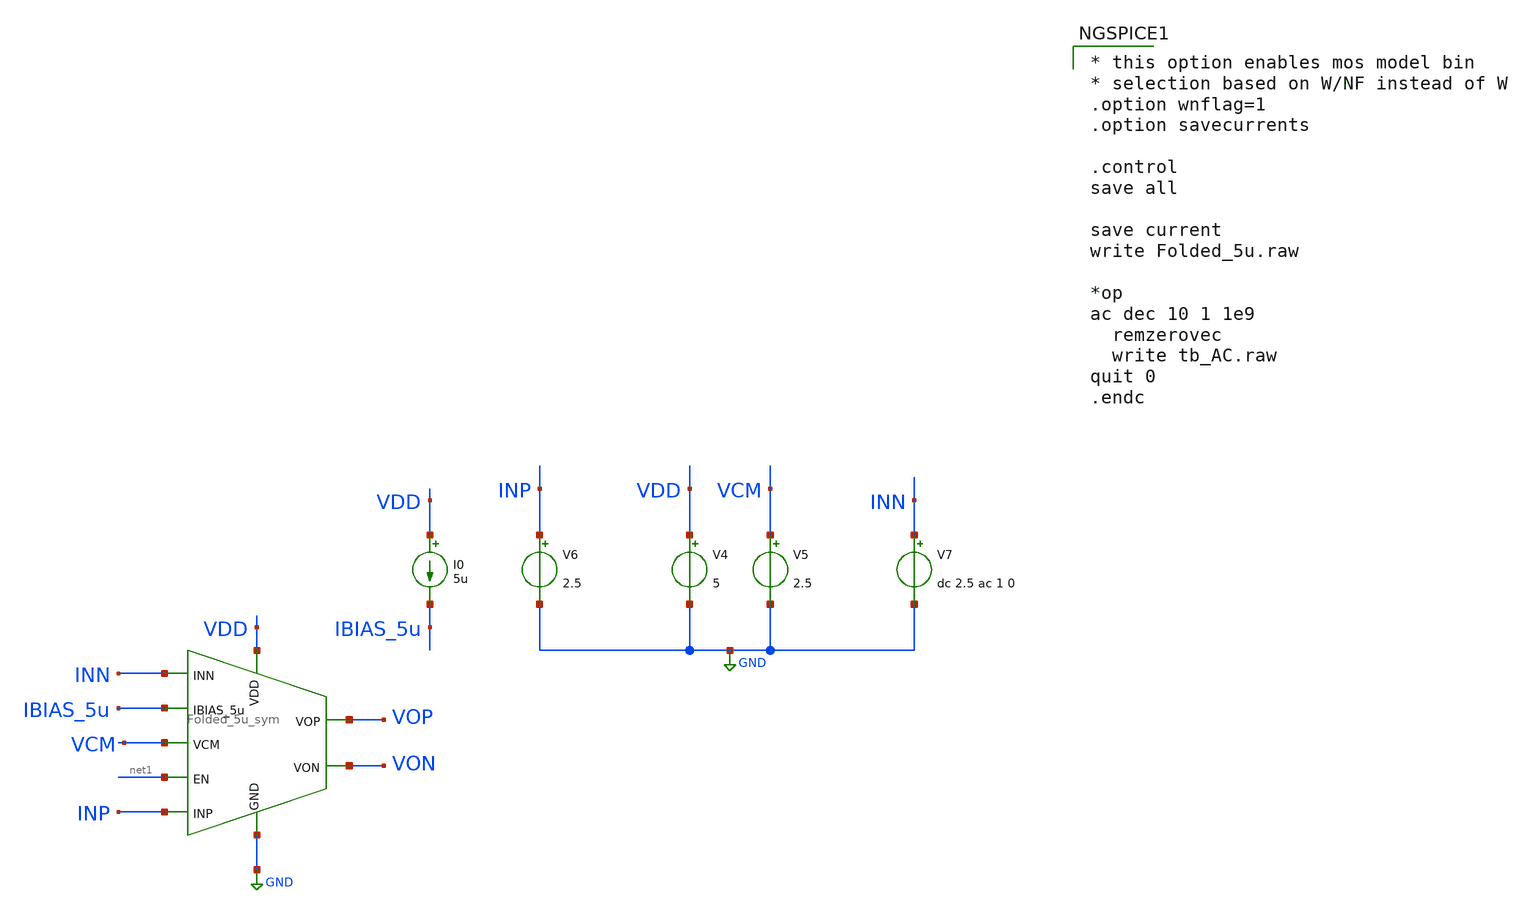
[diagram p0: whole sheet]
** sch_path: Xschem_UPDATE/tb_AC.sch
**.subckt tb_AC
x1 VDD VCM INN INP VOP VON IBIAS_5u net1 GND Folded_5u_sym
I0 VDD IBIAS_5u 5u
V4 VDD GND 5
V6 INP GND 2.5
V5 VCM GND 2.5
V7 INN GND dc 2.5 ac 1 0
**** begin user architecture code

* this option enables mos model bin
* selection based on W/NF instead of W
.option wnflag=1
.option savecurrents

.control
save all

save current
write Folded_5u.raw

*op
ac dec 10 1 1e9
  remzerovec
  write tb_AC.raw
quit 0
.endc


**** end user architecture code
**.ends

* expanding   symbol:  /home/truong/Truong_schem/Folded_5u_sym.sym # of pins=9
** sym_path: Xschem/Folded_5u_sym.sym
** sch_path: Xschem/Folded_5u_sym.sch
.subckt Folded_5u_sym VDD VCM INN INP VOP VON IBIAS_5u EN GND
*.opin VOP
*.opin VON
*.ipin VDD
*.ipin GND
*.ipin IBIAS_5u
*.ipin EN
*.ipin INN
*.ipin INP
*.ipin VCM
*.ipin GND
*.ipin GND
*.ipin GND
*.ipin GND
*.ipin GND
*.ipin IBIAS_5u
*.ipin IBIAS_5u
*.ipin IBIAS_5u
*.ipin VDD
*.ipin VDD
*.ipin VDD
*.ipin VDD
*.ipin VDD
XM13 D13 D13 GND GND sky130_fd_pr__nfet_g5v0d10v5 L=5 W=8 nf=1 ad='int((nf+1)/2) * W/nf * 0.29' as='int((nf+2)/2) * W/nf * 0.29'
+ pd='2*int((nf+1)/2) * (W/nf + 0.29)' ps='2*int((nf+2)/2) * (W/nf + 0.29)' nrd='0.29 / W' nrs='0.29 / W'
+ sa=0 sb=0 sd=0 mult=2 m=2
XM12 VB2 IBIAS_5u GND GND sky130_fd_pr__nfet_g5v0d10v5 L=12 W=2 nf=1 ad='int((nf+1)/2) * W/nf * 0.29'
+ as='int((nf+2)/2) * W/nf * 0.29' pd='2*int((nf+1)/2) * (W/nf + 0.29)' ps='2*int((nf+2)/2) * (W/nf + 0.29)'
+ nrd='0.29 / W' nrs='0.29 / W' sa=0 sb=0 sd=0 mult=2 m=2
XM18 IBIAS_5u IBIAS_5u GND GND sky130_fd_pr__nfet_g5v0d10v5 L=12 W=2 nf=1 ad='int((nf+1)/2) * W/nf * 0.29'
+ as='int((nf+2)/2) * W/nf * 0.29' pd='2*int((nf+1)/2) * (W/nf + 0.29)' ps='2*int((nf+2)/2) * (W/nf + 0.29)'
+ nrd='0.29 / W' nrs='0.29 / W' sa=0 sb=0 sd=0 mult=2 m=2
XM15 VB2 VB2 VB VDD sky130_fd_pr__pfet_g5v0d10v5 L=20 W=10 nf=1 ad='int((nf+1)/2) * W/nf * 0.29' as='int((nf+2)/2) * W/nf * 0.29'
+ pd='2*int((nf+1)/2) * (W/nf + 0.29)' ps='2*int((nf+2)/2) * (W/nf + 0.29)' nrd='0.29 / W' nrs='0.29 / W'
+ sa=0 sb=0 sd=0 mult=32 m=32
XM16 VB VB VDD VDD sky130_fd_pr__pfet_g5v0d10v5 L=2 W=10 nf=1 ad='int((nf+1)/2) * W/nf * 0.29' as='int((nf+2)/2) * W/nf * 0.29'
+ pd='2*int((nf+1)/2) * (W/nf + 0.29)' ps='2*int((nf+2)/2) * (W/nf + 0.29)' nrd='0.29 / W' nrs='0.29 / W'
+ sa=0 sb=0 sd=0 mult=2 m=2
XM17 D17 VB VDD VDD sky130_fd_pr__pfet_g5v0d10v5 L=2 W=10 nf=1 ad='int((nf+1)/2) * W/nf * 0.29' as='int((nf+2)/2) * W/nf * 0.29'
+ pd='2*int((nf+1)/2) * (W/nf + 0.29)' ps='2*int((nf+2)/2) * (W/nf + 0.29)' nrd='0.29 / W' nrs='0.29 / W'
+ sa=0 sb=0 sd=0 mult=2 m=2
XM14 VB3 VB2 D17 VDD sky130_fd_pr__pfet_g5v0d10v5 L=20 W=10 nf=1 ad='int((nf+1)/2) * W/nf * 0.29' as='int((nf+2)/2) * W/nf * 0.29'
+ pd='2*int((nf+1)/2) * (W/nf + 0.29)' ps='2*int((nf+2)/2) * (W/nf + 0.29)' nrd='0.29 / W' nrs='0.29 / W'
+ sa=0 sb=0 sd=0 mult=32 m=32
XM1 P IBIAS_5u GND GND sky130_fd_pr__nfet_g5v0d10v5 L=12 W=2 nf=1 ad='int((nf+1)/2) * W/nf * 0.29' as='int((nf+2)/2) * W/nf * 0.29'
+ pd='2*int((nf+1)/2) * (W/nf + 0.29)' ps='2*int((nf+2)/2) * (W/nf + 0.29)' nrd='0.29 / W' nrs='0.29 / W'
+ sa=0 sb=0 sd=0 mult=160 m=160
XM2 A INN P GND sky130_fd_pr__nfet_g5v0d10v5 L=1 W=80 nf=10 ad='int((nf+1)/2) * W/nf * 0.29' as='int((nf+2)/2) * W/nf * 0.29'
+ pd='2*int((nf+1)/2) * (W/nf + 0.29)' ps='2*int((nf+2)/2) * (W/nf + 0.29)' nrd='0.29 / W' nrs='0.29 / W'
+ sa=0 sb=0 sd=0 mult=20 m=20
XM11 net1 INP P GND sky130_fd_pr__nfet_g5v0d10v5 L=1 W=80 nf=10 ad='int((nf+1)/2) * W/nf * 0.29' as='int((nf+2)/2) * W/nf * 0.29'
+ pd='2*int((nf+1)/2) * (W/nf + 0.29)' ps='2*int((nf+2)/2) * (W/nf + 0.29)' nrd='0.29 / W' nrs='0.29 / W'
+ sa=0 sb=0 sd=0 mult=20 m=20
XM20 net1 VB1 VDD VDD sky130_fd_pr__pfet_g5v0d10v5 L=16 W=2 nf=1 ad='int((nf+1)/2) * W/nf * 0.29' as='int((nf+2)/2) * W/nf * 0.29'
+ pd='2*int((nf+1)/2) * (W/nf + 0.29)' ps='2*int((nf+2)/2) * (W/nf + 0.29)' nrd='0.29 / W' nrs='0.29 / W'
+ sa=0 sb=0 sd=0 mult=164 m=164
XM9 A VB1 VDD VDD sky130_fd_pr__pfet_g5v0d10v5 L=16 W=2 nf=1 ad='int((nf+1)/2) * W/nf * 0.29' as='int((nf+2)/2) * W/nf * 0.29'
+ pd='2*int((nf+1)/2) * (W/nf + 0.29)' ps='2*int((nf+2)/2) * (W/nf + 0.29)' nrd='0.29 / W' nrs='0.29 / W'
+ sa=0 sb=0 sd=0 mult=164 m=164
XM7 net3 VB2 net1 VDD sky130_fd_pr__pfet_g5v0d10v5 L=20 W=10 nf=1 ad='int((nf+1)/2) * W/nf * 0.29' as='int((nf+2)/2) * W/nf * 0.29'
+ pd='2*int((nf+1)/2) * (W/nf + 0.29)' ps='2*int((nf+2)/2) * (W/nf + 0.29)' nrd='0.29 / W' nrs='0.29 / W'
+ sa=0 sb=0 sd=0 mult=32 m=32
XM8 net2 VB2 A VDD sky130_fd_pr__pfet_g5v0d10v5 L=20 W=10 nf=1 ad='int((nf+1)/2) * W/nf * 0.29' as='int((nf+2)/2) * W/nf * 0.29'
+ pd='2*int((nf+1)/2) * (W/nf + 0.29)' ps='2*int((nf+2)/2) * (W/nf + 0.29)' nrd='0.29 / W' nrs='0.29 / W'
+ sa=0 sb=0 sd=0 mult=32 m=32
XM3 P2 IBIAS_5u GND GND sky130_fd_pr__nfet_g5v0d10v5 L=12 W=2 nf=1 ad='int((nf+1)/2) * W/nf * 0.29' as='int((nf+2)/2) * W/nf * 0.29'
+ pd='2*int((nf+1)/2) * (W/nf + 0.29)' ps='2*int((nf+2)/2) * (W/nf + 0.29)' nrd='0.29 / W' nrs='0.29 / W'
+ sa=0 sb=0 sd=0 mult=82 m=82
XM4 P1 IBIAS_5u GND GND sky130_fd_pr__nfet_g5v0d10v5 L=12 W=2 nf=1 ad='int((nf+1)/2) * W/nf * 0.29' as='int((nf+2)/2) * W/nf * 0.29'
+ pd='2*int((nf+1)/2) * (W/nf + 0.29)' ps='2*int((nf+2)/2) * (W/nf + 0.29)' nrd='0.29 / W' nrs='0.29 / W'
+ sa=0 sb=0 sd=0 mult=82 m=82
XM5 net2 VB3 P1 GND sky130_fd_pr__nfet_g5v0d10v5 L=20 W=4 nf=1 ad='int((nf+1)/2) * W/nf * 0.29' as='int((nf+2)/2) * W/nf * 0.29'
+ pd='2*int((nf+1)/2) * (W/nf + 0.29)' ps='2*int((nf+2)/2) * (W/nf + 0.29)' nrd='0.29 / W' nrs='0.29 / W'
+ sa=0 sb=0 sd=0 mult=4 m=4
XM6 net3 VB3 P2 GND sky130_fd_pr__nfet_g5v0d10v5 L=20 W=4 nf=1 ad='int((nf+1)/2) * W/nf * 0.29' as='int((nf+2)/2) * W/nf * 0.29'
+ pd='2*int((nf+1)/2) * (W/nf + 0.29)' ps='2*int((nf+2)/2) * (W/nf + 0.29)' nrd='0.29 / W' nrs='0.29 / W'
+ sa=0 sb=0 sd=0 mult=4 m=4
XM10 VB3 VB3 D13 GND sky130_fd_pr__nfet_g5v0d10v5 L=20 W=4 nf=1 ad='int((nf+1)/2) * W/nf * 0.29' as='int((nf+2)/2) * W/nf * 0.29'
+ pd='2*int((nf+1)/2) * (W/nf + 0.29)' ps='2*int((nf+2)/2) * (W/nf + 0.29)' nrd='0.29 / W' nrs='0.29 / W'
+ sa=0 sb=0 sd=0 mult=4 m=4
XM19 VB1 VB1 VDD VDD sky130_fd_pr__pfet_g5v0d10v5 L=16 W=2 nf=1 ad='int((nf+1)/2) * W/nf * 0.29' as='int((nf+2)/2) * W/nf * 0.29'
+ pd='2*int((nf+1)/2) * (W/nf + 0.29)' ps='2*int((nf+2)/2) * (W/nf + 0.29)' nrd='0.29 / W' nrs='0.29 / W'
+ sa=0 sb=0 sd=0 mult=4 m=4
XM21 net4 net4 VDD VDD sky130_fd_pr__pfet_g5v0d10v5 L=16 W=2 nf=1 ad='int((nf+1)/2) * W/nf * 0.29' as='int((nf+2)/2) * W/nf * 0.29'
+ pd='2*int((nf+1)/2) * (W/nf + 0.29)' ps='2*int((nf+2)/2) * (W/nf + 0.29)' nrd='0.29 / W' nrs='0.29 / W'
+ sa=0 sb=0 sd=0 mult=4 m=4
XM22 VB1 VCM net5 GND sky130_fd_pr__nfet_g5v0d10v5 L=12 W=4 nf=2 ad='int((nf+1)/2) * W/nf * 0.29' as='int((nf+2)/2) * W/nf * 0.29'
+ pd='2*int((nf+1)/2) * (W/nf + 0.29)' ps='2*int((nf+2)/2) * (W/nf + 0.29)' nrd='0.29 / W' nrs='0.29 / W'
+ sa=0 sb=0 sd=0 mult=2 m=2
XM24 net4 VOP net6 GND sky130_fd_pr__nfet_g5v0d10v5 L=12 W=4 nf=2 ad='int((nf+1)/2) * W/nf * 0.29' as='int((nf+2)/2) * W/nf * 0.29'
+ pd='2*int((nf+1)/2) * (W/nf + 0.29)' ps='2*int((nf+2)/2) * (W/nf + 0.29)' nrd='0.29 / W' nrs='0.29 / W'
+ sa=0 sb=0 sd=0 mult=2 m=2
XM25 net4 VON net5 GND sky130_fd_pr__nfet_g5v0d10v5 L=12 W=4 nf=2 ad='int((nf+1)/2) * W/nf * 0.29' as='int((nf+2)/2) * W/nf * 0.29'
+ pd='2*int((nf+1)/2) * (W/nf + 0.29)' ps='2*int((nf+2)/2) * (W/nf + 0.29)' nrd='0.29 / W' nrs='0.29 / W'
+ sa=0 sb=0 sd=0 mult=2 m=2
XM26 net6 IBIAS_5u GND GND sky130_fd_pr__nfet_g5v0d10v5 L=12 W=2 nf=1 ad='int((nf+1)/2) * W/nf * 0.29'
+ as='int((nf+2)/2) * W/nf * 0.29' pd='2*int((nf+1)/2) * (W/nf + 0.29)' ps='2*int((nf+2)/2) * (W/nf + 0.29)'
+ nrd='0.29 / W' nrs='0.29 / W' sa=0 sb=0 sd=0 mult=2 m=2
XM27 net5 IBIAS_5u GND GND sky130_fd_pr__nfet_g5v0d10v5 L=12 W=2 nf=1 ad='int((nf+1)/2) * W/nf * 0.29'
+ as='int((nf+2)/2) * W/nf * 0.29' pd='2*int((nf+1)/2) * (W/nf + 0.29)' ps='2*int((nf+2)/2) * (W/nf + 0.29)'
+ nrd='0.29 / W' nrs='0.29 / W' sa=0 sb=0 sd=0 mult=2 m=2
XM23 VB1 VCM net6 GND sky130_fd_pr__nfet_g5v0d10v5 L=12 W=4 nf=2 ad='int((nf+1)/2) * W/nf * 0.29' as='int((nf+2)/2) * W/nf * 0.29'
+ pd='2*int((nf+1)/2) * (W/nf + 0.29)' ps='2*int((nf+2)/2) * (W/nf + 0.29)' nrd='0.29 / W' nrs='0.29 / W'
+ sa=0 sb=0 sd=0 mult=2 m=2
XM30 P2 INP net7 VDD sky130_fd_pr__pfet_g5v0d10v5 L=10 W=60 nf=1 ad='int((nf+1)/2) * W/nf * 0.29' as='int((nf+2)/2) * W/nf * 0.29'
+ pd='2*int((nf+1)/2) * (W/nf + 0.29)' ps='2*int((nf+2)/2) * (W/nf + 0.29)' nrd='0.29 / W' nrs='0.29 / W'
+ sa=0 sb=0 sd=0 mult=20 m=20
XM31 P1 INN net7 VDD sky130_fd_pr__pfet_g5v0d10v5 L=10 W=60 nf=1 ad='int((nf+1)/2) * W/nf * 0.29' as='int((nf+2)/2) * W/nf * 0.29'
+ pd='2*int((nf+1)/2) * (W/nf + 0.29)' ps='2*int((nf+2)/2) * (W/nf + 0.29)' nrd='0.29 / W' nrs='0.29 / W'
+ sa=0 sb=0 sd=0 mult=20 m=20
XM28 net7 VB VDD VDD sky130_fd_pr__pfet_g5v0d10v5 L=2 W=10 nf=1 ad='int((nf+1)/2) * W/nf * 0.29' as='int((nf+2)/2) * W/nf * 0.29'
+ pd='2*int((nf+1)/2) * (W/nf + 0.29)' ps='2*int((nf+2)/2) * (W/nf + 0.29)' nrd='0.29 / W' nrs='0.29 / W'
+ sa=0 sb=0 sd=0 mult=160 m=160
XM29 VDD net3 VOP GND sky130_fd_pr__nfet_g5v0d10v5 L=1 W=50 nf=1 ad='int((nf+1)/2) * W/nf * 0.29' as='int((nf+2)/2) * W/nf * 0.29'
+ pd='2*int((nf+1)/2) * (W/nf + 0.29)' ps='2*int((nf+2)/2) * (W/nf + 0.29)' nrd='0.29 / W' nrs='0.29 / W'
+ sa=0 sb=0 sd=0 mult=10 m=10
R1 GND VOP sky130_fd_pr__res_generic_l1 W=1 L=100000000 m=1
XM32 VDD net2 VON GND sky130_fd_pr__nfet_g5v0d10v5 L=1 W=50 nf=1 ad='int((nf+1)/2) * W/nf * 0.29' as='int((nf+2)/2) * W/nf * 0.29'
+ pd='2*int((nf+1)/2) * (W/nf + 0.29)' ps='2*int((nf+2)/2) * (W/nf + 0.29)' nrd='0.29 / W' nrs='0.29 / W'
+ sa=0 sb=0 sd=0 mult=10 m=10
R2 GND VON sky130_fd_pr__res_generic_l1 W=1 L=100000000 m=1
XM33 IBIAS_5u EN GND GND sky130_fd_pr__nfet_g5v0d10v5 L=12 W=2 nf=1 ad='int((nf+1)/2) * W/nf * 0.29'
+ as='int((nf+2)/2) * W/nf * 0.29' pd='2*int((nf+1)/2) * (W/nf + 0.29)' ps='2*int((nf+2)/2) * (W/nf + 0.29)'
+ nrd='0.29 / W' nrs='0.29 / W' sa=0 sb=0 sd=0 mult=8 m=8
.ends

.GLOBAL GND
.end
